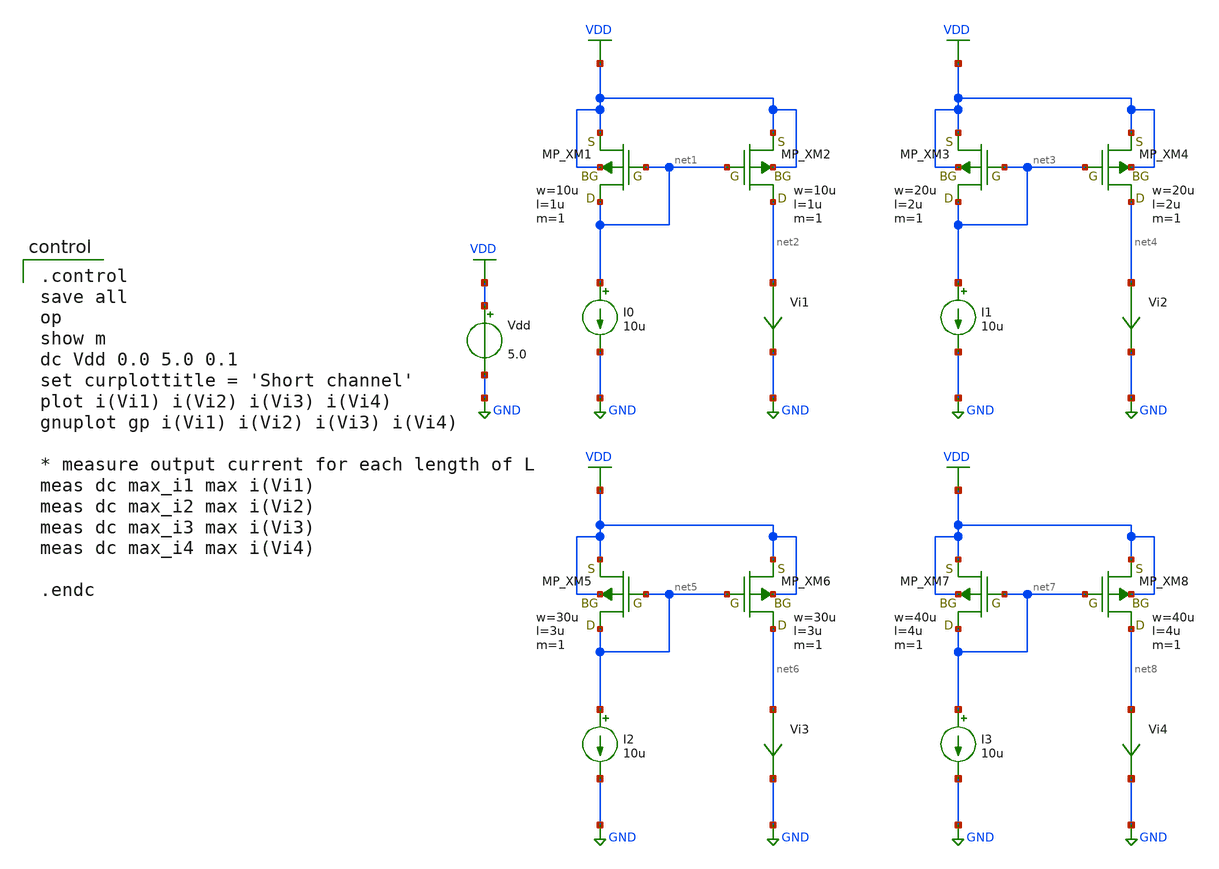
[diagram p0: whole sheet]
** sch_path: member_project/OPAMP/YutakaKOTANI/short_channel.sch
**.subckt short_channel
I0 net1 GND 10u
Vi1 net2 GND 0
.save i(vi1)
Vdd VDD GND 5.0
I1 net3 GND 10u
Vi2 net4 GND 0
.save i(vi2)
XM1 net1 net1 VDD VDD PMOS w=10u l=1u as=0 ad=0 ps=0 pd=0 nrd=0 nrs=0 m=1
XM2 net2 net1 VDD VDD PMOS w=10u l=1u as=0 ad=0 ps=0 pd=0 nrd=0 nrs=0 m=1
XM3 net3 net3 VDD VDD PMOS w=20u l=2u as=0 ad=0 ps=0 pd=0 nrd=0 nrs=0 m=1
XM4 net4 net3 VDD VDD PMOS w=20u l=2u as=0 ad=0 ps=0 pd=0 nrd=0 nrs=0 m=1
I2 net5 GND 10u
Vi3 net6 GND 0
.save i(vi3)
I3 net7 GND 10u
Vi4 net8 GND 0
.save i(vi4)
XM5 net5 net5 VDD VDD PMOS w=30u l=3u as=0 ad=0 ps=0 pd=0 nrd=0 nrs=0 m=1
XM6 net6 net5 VDD VDD PMOS w=30u l=3u as=0 ad=0 ps=0 pd=0 nrd=0 nrs=0 m=1
XM7 net7 net7 VDD VDD PMOS w=40u l=4u as=0 ad=0 ps=0 pd=0 nrd=0 nrs=0 m=1
XM8 net8 net7 VDD VDD PMOS w=40u l=4u as=0 ad=0 ps=0 pd=0 nrd=0 nrs=0 m=1
**** begin user architecture code

.control
save all
op
show m
dc Vdd 0.0 5.0 0.1
set curplottitle = 'Short channel'
plot i(Vi1) i(Vi2) i(Vi3) i(Vi4)
gnuplot gp i(Vi1) i(Vi2) i(Vi3) i(Vi4)

* measure output current for each length of L
meas dc max_i1 max i(Vi1)
meas dc max_i2 max i(Vi2)
meas dc max_i3 max i(Vi3)
meas dc max_i4 max i(Vi4)

.endc

 .include $::LIB/../ip62_models
**** end user architecture code
**.ends
.GLOBAL GND
.GLOBAL VDD
.end
